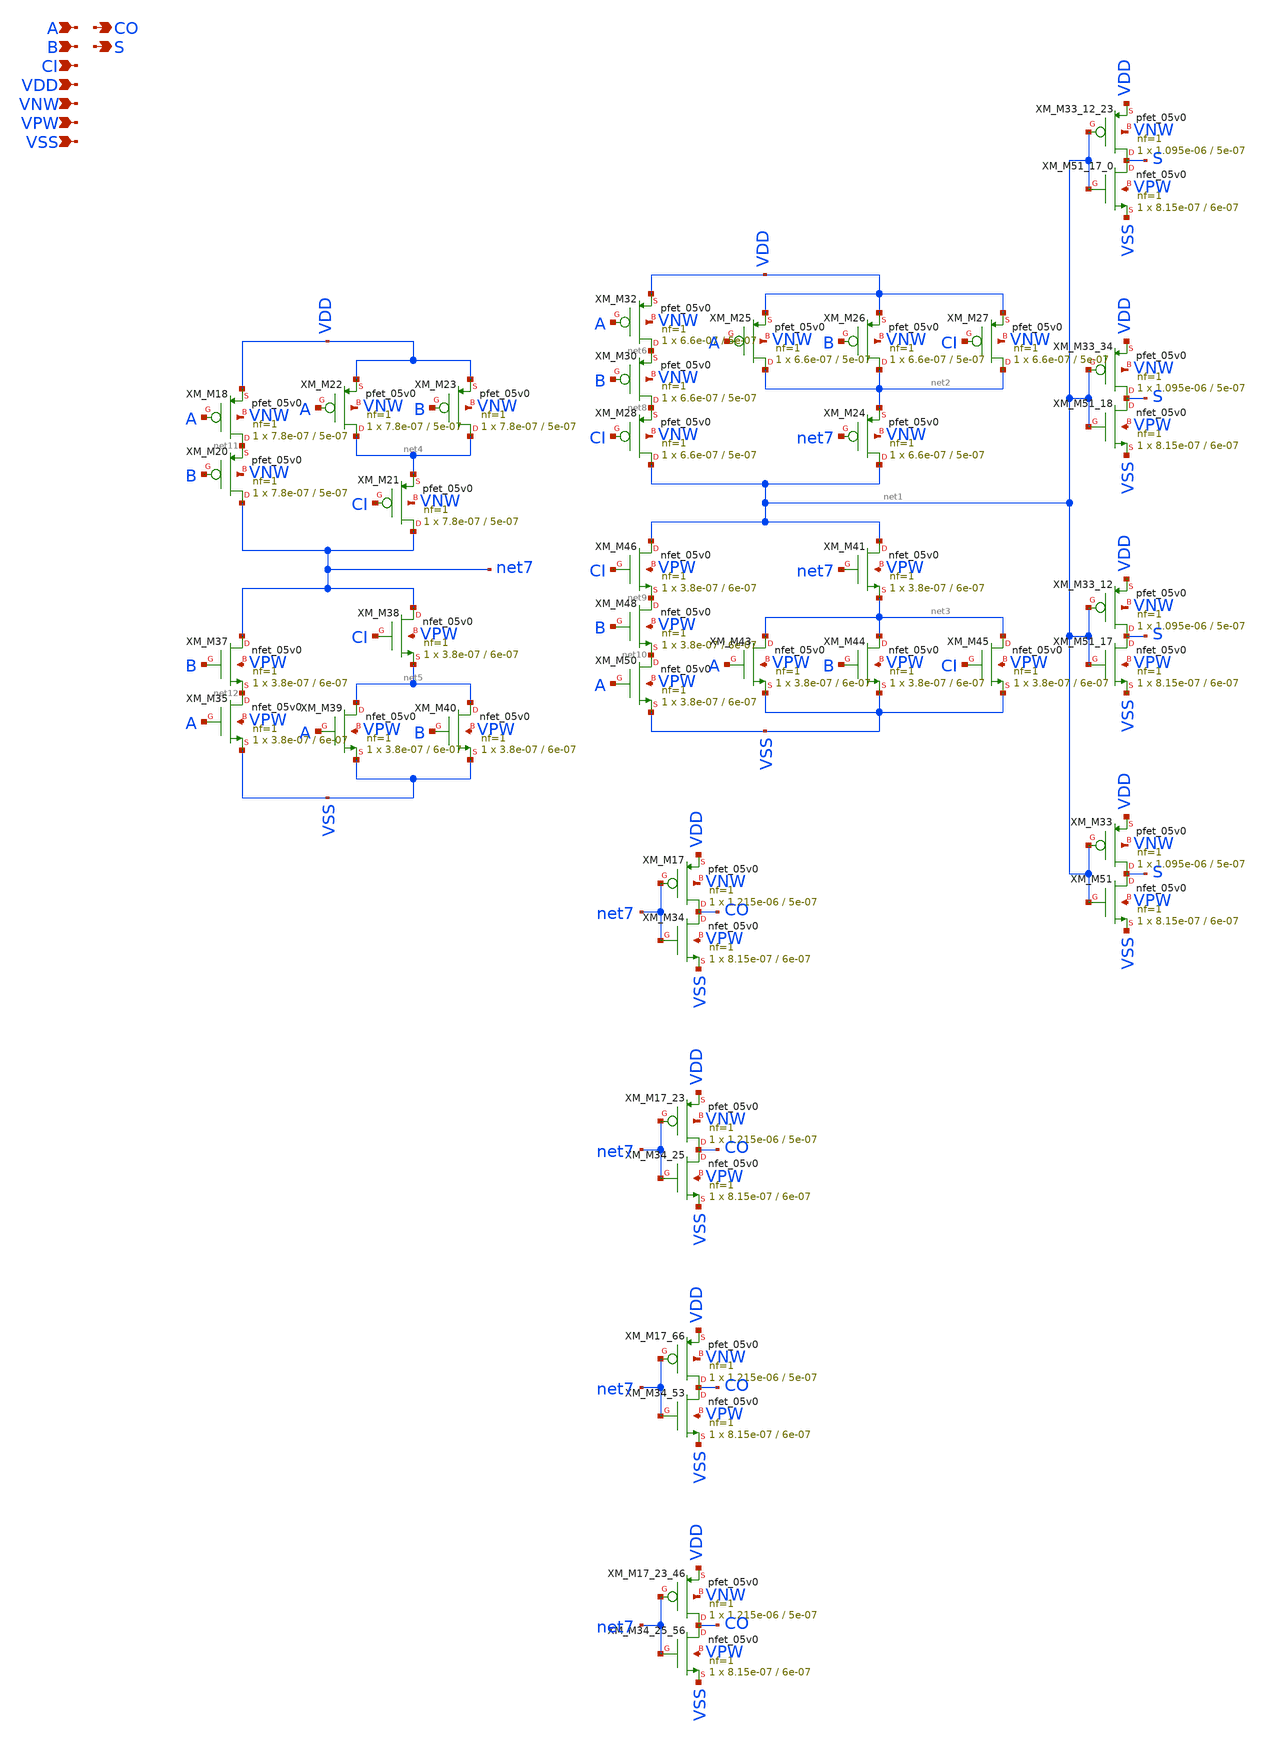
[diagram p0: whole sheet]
** sch_path: schematics/addf/gf180mcu_fd_sc_mcu7t5v0__addf_4.sch
**.subckt gf180mcu_fd_sc_mcu7t5v0__addf_4 A B CI CO S VDD VNW VPW VSS
*.ipin A
*.ipin B
*.ipin CI
*.opin CO
*.opin S
*.ipin VDD
*.ipin VNW
*.ipin VPW
*.ipin VSS
XM_M33_12_23 S net1 VDD VNW pfet_05v0 L=5e-07 W=1.095e-06 nf=1 ad='int((nf+1)/2) * W/nf * 0.18u' as='int((nf+2)/2) * W/nf * 0.18u'
+ pd='2*int((nf+1)/2) * (W/nf + 0.18u)' ps='2*int((nf+2)/2) * (W/nf + 0.18u)' nrd='0.18u / W' nrs='0.18u / W'
+ sa=0 sb=0 sd=0 m=1 par=1
XM_M51_17_0 S net1 VSS VPW nfet_05v0 L=6e-07 W=8.15e-07 nf=1 ad='int((nf+1)/2) * W/nf * 0.18u' as='int((nf+2)/2) * W/nf * 0.18u'
+ pd='2*int((nf+1)/2) * (W/nf + 0.18u)' ps='2*int((nf+2)/2) * (W/nf + 0.18u)' nrd='0.18u / W' nrs='0.18u / W'
+ sa=0 sb=0 sd=0 m=1
XM_M33_34 S net1 VDD VNW pfet_05v0 L=5e-07 W=1.095e-06 nf=1 ad='int((nf+1)/2) * W/nf * 0.18u' as='int((nf+2)/2) * W/nf * 0.18u'
+ pd='2*int((nf+1)/2) * (W/nf + 0.18u)' ps='2*int((nf+2)/2) * (W/nf + 0.18u)' nrd='0.18u / W' nrs='0.18u / W'
+ sa=0 sb=0 sd=0 m=1 par=1
XM_M51_18 S net1 VSS VPW nfet_05v0 L=6e-07 W=8.15e-07 nf=1 ad='int((nf+1)/2) * W/nf * 0.18u' as='int((nf+2)/2) * W/nf * 0.18u'
+ pd='2*int((nf+1)/2) * (W/nf + 0.18u)' ps='2*int((nf+2)/2) * (W/nf + 0.18u)' nrd='0.18u / W' nrs='0.18u / W'
+ sa=0 sb=0 sd=0 m=1
XM_M33_12 S net1 VDD VNW pfet_05v0 L=5e-07 W=1.095e-06 nf=1 ad='int((nf+1)/2) * W/nf * 0.18u' as='int((nf+2)/2) * W/nf * 0.18u'
+ pd='2*int((nf+1)/2) * (W/nf + 0.18u)' ps='2*int((nf+2)/2) * (W/nf + 0.18u)' nrd='0.18u / W' nrs='0.18u / W'
+ sa=0 sb=0 sd=0 m=1 par=1
XM_M51_17 S net1 VSS VPW nfet_05v0 L=6e-07 W=8.15e-07 nf=1 ad='int((nf+1)/2) * W/nf * 0.18u' as='int((nf+2)/2) * W/nf * 0.18u'
+ pd='2*int((nf+1)/2) * (W/nf + 0.18u)' ps='2*int((nf+2)/2) * (W/nf + 0.18u)' nrd='0.18u / W' nrs='0.18u / W'
+ sa=0 sb=0 sd=0 m=1
XM_M33 S net1 VDD VNW pfet_05v0 L=5e-07 W=1.095e-06 nf=1 ad='int((nf+1)/2) * W/nf * 0.18u' as='int((nf+2)/2) * W/nf * 0.18u'
+ pd='2*int((nf+1)/2) * (W/nf + 0.18u)' ps='2*int((nf+2)/2) * (W/nf + 0.18u)' nrd='0.18u / W' nrs='0.18u / W'
+ sa=0 sb=0 sd=0 m=1 par=1
XM_M51 S net1 VSS VPW nfet_05v0 L=6e-07 W=8.15e-07 nf=1 ad='int((nf+1)/2) * W/nf * 0.18u' as='int((nf+2)/2) * W/nf * 0.18u'
+ pd='2*int((nf+1)/2) * (W/nf + 0.18u)' ps='2*int((nf+2)/2) * (W/nf + 0.18u)' nrd='0.18u / W' nrs='0.18u / W'
+ sa=0 sb=0 sd=0 m=1
XM_M32 net6 A VDD VNW pfet_05v0 L=5e-07 W=6.6e-07 nf=1 ad='int((nf+1)/2) * W/nf * 0.18u' as='int((nf+2)/2) * W/nf * 0.18u'
+ pd='2*int((nf+1)/2) * (W/nf + 0.18u)' ps='2*int((nf+2)/2) * (W/nf + 0.18u)' nrd='0.18u / W' nrs='0.18u / W'
+ sa=0 sb=0 sd=0 m=1 par=1
XM_M30 net8 B net6 VNW pfet_05v0 L=5e-07 W=6.6e-07 nf=1 ad='int((nf+1)/2) * W/nf * 0.18u' as='int((nf+2)/2) * W/nf * 0.18u'
+ pd='2*int((nf+1)/2) * (W/nf + 0.18u)' ps='2*int((nf+2)/2) * (W/nf + 0.18u)' nrd='0.18u / W' nrs='0.18u / W'
+ sa=0 sb=0 sd=0 m=1 par=1
XM_M28 net1 CI net8 VNW pfet_05v0 L=5e-07 W=6.6e-07 nf=1 ad='int((nf+1)/2) * W/nf * 0.18u' as='int((nf+2)/2) * W/nf * 0.18u'
+ pd='2*int((nf+1)/2) * (W/nf + 0.18u)' ps='2*int((nf+2)/2) * (W/nf + 0.18u)' nrd='0.18u / W' nrs='0.18u / W'
+ sa=0 sb=0 sd=0 m=1 par=1
XM_M25 net2 A VDD VNW pfet_05v0 L=5e-07 W=6.6e-07 nf=1 ad='int((nf+1)/2) * W/nf * 0.18u' as='int((nf+2)/2) * W/nf * 0.18u'
+ pd='2*int((nf+1)/2) * (W/nf + 0.18u)' ps='2*int((nf+2)/2) * (W/nf + 0.18u)' nrd='0.18u / W' nrs='0.18u / W'
+ sa=0 sb=0 sd=0 m=1 par=1
XM_M26 net2 B VDD VNW pfet_05v0 L=5e-07 W=6.6e-07 nf=1 ad='int((nf+1)/2) * W/nf * 0.18u' as='int((nf+2)/2) * W/nf * 0.18u'
+ pd='2*int((nf+1)/2) * (W/nf + 0.18u)' ps='2*int((nf+2)/2) * (W/nf + 0.18u)' nrd='0.18u / W' nrs='0.18u / W'
+ sa=0 sb=0 sd=0 m=1 par=1
XM_M27 net2 CI VDD VNW pfet_05v0 L=5e-07 W=6.6e-07 nf=1 ad='int((nf+1)/2) * W/nf * 0.18u' as='int((nf+2)/2) * W/nf * 0.18u'
+ pd='2*int((nf+1)/2) * (W/nf + 0.18u)' ps='2*int((nf+2)/2) * (W/nf + 0.18u)' nrd='0.18u / W' nrs='0.18u / W'
+ sa=0 sb=0 sd=0 m=1 par=1
XM_M24 net1 net7 net2 VNW pfet_05v0 L=5e-07 W=6.6e-07 nf=1 ad='int((nf+1)/2) * W/nf * 0.18u' as='int((nf+2)/2) * W/nf * 0.18u'
+ pd='2*int((nf+1)/2) * (W/nf + 0.18u)' ps='2*int((nf+2)/2) * (W/nf + 0.18u)' nrd='0.18u / W' nrs='0.18u / W'
+ sa=0 sb=0 sd=0 m=1 par=1
XM_M46 net1 CI net9 VPW nfet_05v0 L=6e-07 W=3.8e-07 nf=1 ad='int((nf+1)/2) * W/nf * 0.18u' as='int((nf+2)/2) * W/nf * 0.18u'
+ pd='2*int((nf+1)/2) * (W/nf + 0.18u)' ps='2*int((nf+2)/2) * (W/nf + 0.18u)' nrd='0.18u / W' nrs='0.18u / W'
+ sa=0 sb=0 sd=0 m=1
XM_M48 net9 B net10 VPW nfet_05v0 L=6e-07 W=3.8e-07 nf=1 ad='int((nf+1)/2) * W/nf * 0.18u' as='int((nf+2)/2) * W/nf * 0.18u'
+ pd='2*int((nf+1)/2) * (W/nf + 0.18u)' ps='2*int((nf+2)/2) * (W/nf + 0.18u)' nrd='0.18u / W' nrs='0.18u / W'
+ sa=0 sb=0 sd=0 m=1
XM_M50 net10 A VSS VPW nfet_05v0 L=6e-07 W=3.8e-07 nf=1 ad='int((nf+1)/2) * W/nf * 0.18u' as='int((nf+2)/2) * W/nf * 0.18u'
+ pd='2*int((nf+1)/2) * (W/nf + 0.18u)' ps='2*int((nf+2)/2) * (W/nf + 0.18u)' nrd='0.18u / W' nrs='0.18u / W'
+ sa=0 sb=0 sd=0 m=1
XM_M41 net1 net7 net3 VPW nfet_05v0 L=6e-07 W=3.8e-07 nf=1 ad='int((nf+1)/2) * W/nf * 0.18u' as='int((nf+2)/2) * W/nf * 0.18u'
+ pd='2*int((nf+1)/2) * (W/nf + 0.18u)' ps='2*int((nf+2)/2) * (W/nf + 0.18u)' nrd='0.18u / W' nrs='0.18u / W'
+ sa=0 sb=0 sd=0 m=1
XM_M43 net3 A VSS VPW nfet_05v0 L=6e-07 W=3.8e-07 nf=1 ad='int((nf+1)/2) * W/nf * 0.18u' as='int((nf+2)/2) * W/nf * 0.18u'
+ pd='2*int((nf+1)/2) * (W/nf + 0.18u)' ps='2*int((nf+2)/2) * (W/nf + 0.18u)' nrd='0.18u / W' nrs='0.18u / W'
+ sa=0 sb=0 sd=0 m=1
XM_M44 net3 B VSS VPW nfet_05v0 L=6e-07 W=3.8e-07 nf=1 ad='int((nf+1)/2) * W/nf * 0.18u' as='int((nf+2)/2) * W/nf * 0.18u'
+ pd='2*int((nf+1)/2) * (W/nf + 0.18u)' ps='2*int((nf+2)/2) * (W/nf + 0.18u)' nrd='0.18u / W' nrs='0.18u / W'
+ sa=0 sb=0 sd=0 m=1
XM_M45 net3 CI VSS VPW nfet_05v0 L=6e-07 W=3.8e-07 nf=1 ad='int((nf+1)/2) * W/nf * 0.18u' as='int((nf+2)/2) * W/nf * 0.18u'
+ pd='2*int((nf+1)/2) * (W/nf + 0.18u)' ps='2*int((nf+2)/2) * (W/nf + 0.18u)' nrd='0.18u / W' nrs='0.18u / W'
+ sa=0 sb=0 sd=0 m=1
XM_M18 net11 A VDD VNW pfet_05v0 L=5e-07 W=7.8e-07 nf=1 ad='int((nf+1)/2) * W/nf * 0.18u' as='int((nf+2)/2) * W/nf * 0.18u'
+ pd='2*int((nf+1)/2) * (W/nf + 0.18u)' ps='2*int((nf+2)/2) * (W/nf + 0.18u)' nrd='0.18u / W' nrs='0.18u / W'
+ sa=0 sb=0 sd=0 m=1 par=1
XM_M20 net7 B net11 VNW pfet_05v0 L=5e-07 W=7.8e-07 nf=1 ad='int((nf+1)/2) * W/nf * 0.18u' as='int((nf+2)/2) * W/nf * 0.18u'
+ pd='2*int((nf+1)/2) * (W/nf + 0.18u)' ps='2*int((nf+2)/2) * (W/nf + 0.18u)' nrd='0.18u / W' nrs='0.18u / W'
+ sa=0 sb=0 sd=0 m=1 par=1
XM_M22 net4 A VDD VNW pfet_05v0 L=5e-07 W=7.8e-07 nf=1 ad='int((nf+1)/2) * W/nf * 0.18u' as='int((nf+2)/2) * W/nf * 0.18u'
+ pd='2*int((nf+1)/2) * (W/nf + 0.18u)' ps='2*int((nf+2)/2) * (W/nf + 0.18u)' nrd='0.18u / W' nrs='0.18u / W'
+ sa=0 sb=0 sd=0 m=1 par=1
XM_M23 net4 B VDD VNW pfet_05v0 L=5e-07 W=7.8e-07 nf=1 ad='int((nf+1)/2) * W/nf * 0.18u' as='int((nf+2)/2) * W/nf * 0.18u'
+ pd='2*int((nf+1)/2) * (W/nf + 0.18u)' ps='2*int((nf+2)/2) * (W/nf + 0.18u)' nrd='0.18u / W' nrs='0.18u / W'
+ sa=0 sb=0 sd=0 m=1 par=1
XM_M21 net7 CI net4 VNW pfet_05v0 L=5e-07 W=7.8e-07 nf=1 ad='int((nf+1)/2) * W/nf * 0.18u' as='int((nf+2)/2) * W/nf * 0.18u'
+ pd='2*int((nf+1)/2) * (W/nf + 0.18u)' ps='2*int((nf+2)/2) * (W/nf + 0.18u)' nrd='0.18u / W' nrs='0.18u / W'
+ sa=0 sb=0 sd=0 m=1 par=1
XM_M37 net7 B net12 VPW nfet_05v0 L=6e-07 W=3.8e-07 nf=1 ad='int((nf+1)/2) * W/nf * 0.18u' as='int((nf+2)/2) * W/nf * 0.18u'
+ pd='2*int((nf+1)/2) * (W/nf + 0.18u)' ps='2*int((nf+2)/2) * (W/nf + 0.18u)' nrd='0.18u / W' nrs='0.18u / W'
+ sa=0 sb=0 sd=0 m=1
XM_M35 net12 A VSS VPW nfet_05v0 L=6e-07 W=3.8e-07 nf=1 ad='int((nf+1)/2) * W/nf * 0.18u' as='int((nf+2)/2) * W/nf * 0.18u'
+ pd='2*int((nf+1)/2) * (W/nf + 0.18u)' ps='2*int((nf+2)/2) * (W/nf + 0.18u)' nrd='0.18u / W' nrs='0.18u / W'
+ sa=0 sb=0 sd=0 m=1
XM_M38 net7 CI net5 VPW nfet_05v0 L=6e-07 W=3.8e-07 nf=1 ad='int((nf+1)/2) * W/nf * 0.18u' as='int((nf+2)/2) * W/nf * 0.18u'
+ pd='2*int((nf+1)/2) * (W/nf + 0.18u)' ps='2*int((nf+2)/2) * (W/nf + 0.18u)' nrd='0.18u / W' nrs='0.18u / W'
+ sa=0 sb=0 sd=0 m=1
XM_M39 net5 A VSS VPW nfet_05v0 L=6e-07 W=3.8e-07 nf=1 ad='int((nf+1)/2) * W/nf * 0.18u' as='int((nf+2)/2) * W/nf * 0.18u'
+ pd='2*int((nf+1)/2) * (W/nf + 0.18u)' ps='2*int((nf+2)/2) * (W/nf + 0.18u)' nrd='0.18u / W' nrs='0.18u / W'
+ sa=0 sb=0 sd=0 m=1
XM_M40 net5 B VSS VPW nfet_05v0 L=6e-07 W=3.8e-07 nf=1 ad='int((nf+1)/2) * W/nf * 0.18u' as='int((nf+2)/2) * W/nf * 0.18u'
+ pd='2*int((nf+1)/2) * (W/nf + 0.18u)' ps='2*int((nf+2)/2) * (W/nf + 0.18u)' nrd='0.18u / W' nrs='0.18u / W'
+ sa=0 sb=0 sd=0 m=1
XM_M17 CO net7 VDD VNW pfet_05v0 L=5e-07 W=1.215e-06 nf=1 ad='int((nf+1)/2) * W/nf * 0.18u' as='int((nf+2)/2) * W/nf * 0.18u'
+ pd='2*int((nf+1)/2) * (W/nf + 0.18u)' ps='2*int((nf+2)/2) * (W/nf + 0.18u)' nrd='0.18u / W' nrs='0.18u / W'
+ sa=0 sb=0 sd=0 m=1 par=1
XM_M34 CO net7 VSS VPW nfet_05v0 L=6e-07 W=8.15e-07 nf=1 ad='int((nf+1)/2) * W/nf * 0.18u' as='int((nf+2)/2) * W/nf * 0.18u'
+ pd='2*int((nf+1)/2) * (W/nf + 0.18u)' ps='2*int((nf+2)/2) * (W/nf + 0.18u)' nrd='0.18u / W' nrs='0.18u / W'
+ sa=0 sb=0 sd=0 m=1
XM_M17_23 CO net7 VDD VNW pfet_05v0 L=5e-07 W=1.215e-06 nf=1 ad='int((nf+1)/2) * W/nf * 0.18u' as='int((nf+2)/2) * W/nf * 0.18u'
+ pd='2*int((nf+1)/2) * (W/nf + 0.18u)' ps='2*int((nf+2)/2) * (W/nf + 0.18u)' nrd='0.18u / W' nrs='0.18u / W'
+ sa=0 sb=0 sd=0 m=1 par=1
XM_M34_25 CO net7 VSS VPW nfet_05v0 L=6e-07 W=8.15e-07 nf=1 ad='int((nf+1)/2) * W/nf * 0.18u' as='int((nf+2)/2) * W/nf * 0.18u'
+ pd='2*int((nf+1)/2) * (W/nf + 0.18u)' ps='2*int((nf+2)/2) * (W/nf + 0.18u)' nrd='0.18u / W' nrs='0.18u / W'
+ sa=0 sb=0 sd=0 m=1
XM_M17_66 CO net7 VDD VNW pfet_05v0 L=5e-07 W=1.215e-06 nf=1 ad='int((nf+1)/2) * W/nf * 0.18u' as='int((nf+2)/2) * W/nf * 0.18u'
+ pd='2*int((nf+1)/2) * (W/nf + 0.18u)' ps='2*int((nf+2)/2) * (W/nf + 0.18u)' nrd='0.18u / W' nrs='0.18u / W'
+ sa=0 sb=0 sd=0 m=1 par=1
XM_M34_53 CO net7 VSS VPW nfet_05v0 L=6e-07 W=8.15e-07 nf=1 ad='int((nf+1)/2) * W/nf * 0.18u' as='int((nf+2)/2) * W/nf * 0.18u'
+ pd='2*int((nf+1)/2) * (W/nf + 0.18u)' ps='2*int((nf+2)/2) * (W/nf + 0.18u)' nrd='0.18u / W' nrs='0.18u / W'
+ sa=0 sb=0 sd=0 m=1
XM_M17_23_46 CO net7 VDD VNW pfet_05v0 L=5e-07 W=1.215e-06 nf=1 ad='int((nf+1)/2) * W/nf * 0.18u' as='int((nf+2)/2) * W/nf * 0.18u'
+ pd='2*int((nf+1)/2) * (W/nf + 0.18u)' ps='2*int((nf+2)/2) * (W/nf + 0.18u)' nrd='0.18u / W' nrs='0.18u / W'
+ sa=0 sb=0 sd=0 m=1 par=1
XM_M34_25_56 CO net7 VSS VPW nfet_05v0 L=6e-07 W=8.15e-07 nf=1 ad='int((nf+1)/2) * W/nf * 0.18u' as='int((nf+2)/2) * W/nf * 0.18u'
+ pd='2*int((nf+1)/2) * (W/nf + 0.18u)' ps='2*int((nf+2)/2) * (W/nf + 0.18u)' nrd='0.18u / W' nrs='0.18u / W'
+ sa=0 sb=0 sd=0 m=1
**.ends
.end
